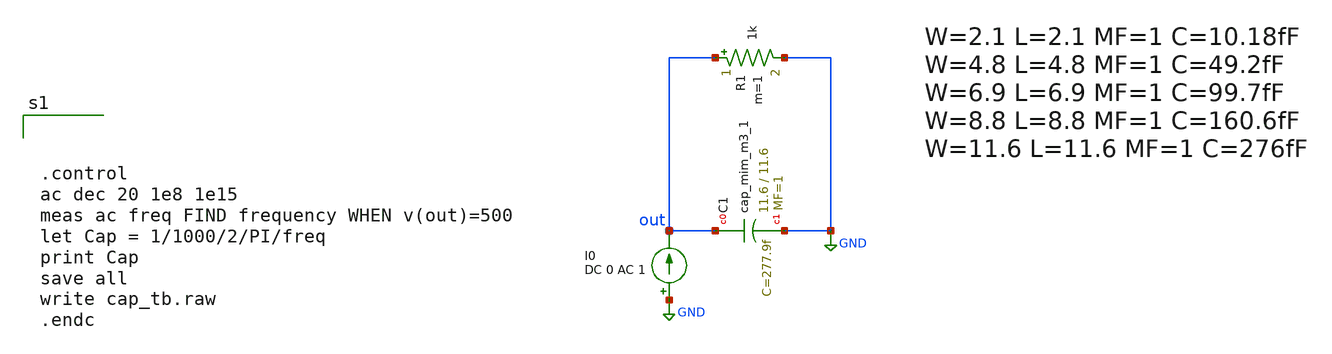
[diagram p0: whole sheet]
** sch_path: verification/schematic/cap_tb.sch
**.subckt cap_tb
I0 GND out DC 0 AC 1
R1 out GND 1k m=1
XC1 out GND sky130_fd_pr__cap_mim_m3_1 W=11.6 L=11.6 MF=1 m=1
**** begin user architecture code

** opencircuitdesign pdks install
.lib /farmshare/home/classes/ee/372/PDKs/open_pdks_1.0.310/sky130/sky130A/libs.tech/ngspice/sky130.lib.spice tt
.inc /farmshare/home/classes/ee/372/PDKs/open_pdks_1.0.310/sky130/sky130A/libs.ref/sky130_fd_sc_hd/spice/sky130_fd_sc_hd.spice




.control
ac dec 20 1e8 1e15
meas ac freq FIND frequency WHEN v(out)=500
let Cap = 1/1000/2/PI/freq
print Cap
save all
write cap_tb.raw
.endc



**** end user architecture code
**.ends
.GLOBAL GND
.end
